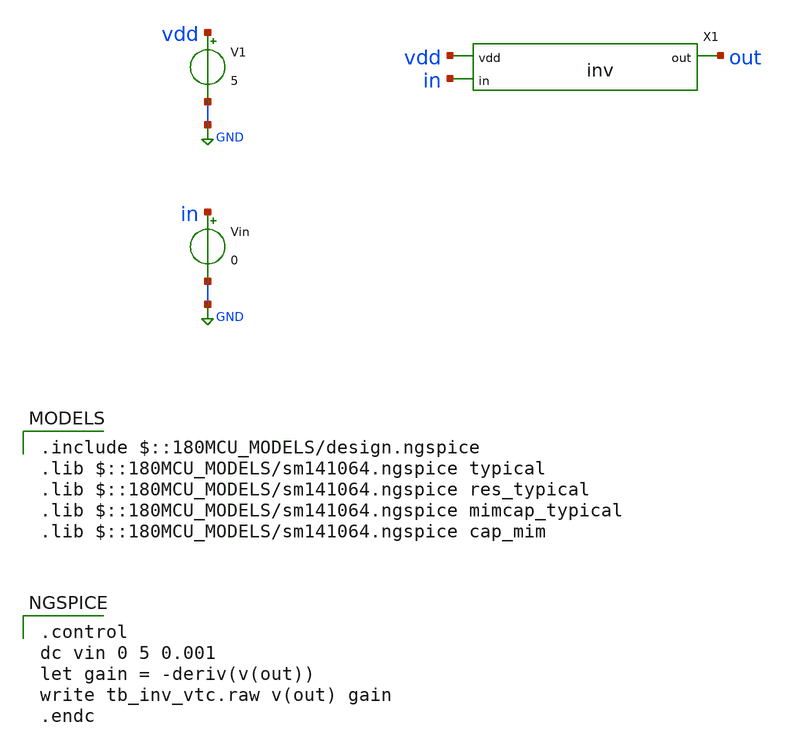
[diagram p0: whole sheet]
** sch_path: Schematics #2/sims/tb/tb_inv_vtc.sch
**.subckt tb_inv_vtc
V1 vdd GND 5
Vin in GND 0
X1 out vdd in inv
**** begin user architecture code
 .include $::180MCU_MODELS/design.ngspice
.lib $::180MCU_MODELS/sm141064.ngspice typical
.lib $::180MCU_MODELS/sm141064.ngspice res_typical
.lib $::180MCU_MODELS/sm141064.ngspice mimcap_typical
.lib $::180MCU_MODELS/sm141064.ngspice cap_mim

.control
dc vin 0 5 0.001
let gain = -deriv(v(out))
write tb_inv_vtc.raw v(out) gain
.endc

**** end user architecture code
**.ends

* expanding   symbol:  xschem/inv.sym # of pins=3
** sym_path: schematic pt2/xschem/inv.sym
** sch_path: schematic pt2/xschem/inv.sch
.subckt inv out vdd in
*.opin out
*.ipin vdd
*.ipin in
XM1 out in gnd GND nfet_03v3 L=0.28u W=wn nf=1 ad='int((nf+1)/2) * W/nf * 0.18u' as='int((nf+2)/2) * W/nf * 0.18u'
+ pd='2*int((nf+1)/2) * (W/nf + 0.18u)' ps='2*int((nf+2)/2) * (W/nf + 0.18u)' nrd='0.18u / W' nrs='0.18u / W'
+ sa=0 sb=0 sd=0 m=1 par=1
XM2 out in vdd VDD pfet_03v3 L=0.28u W=wp nf=1 ad='int((nf+1)/2) * W/nf * 0.18u' as='int((nf+2)/2) * W/nf * 0.18u'
+ pd='2*int((nf+1)/2) * (W/nf + 0.18u)' ps='2*int((nf+2)/2) * (W/nf + 0.18u)' nrd='0.18u / W' nrs='0.18u / W'
+ sa=0 sb=0 sd=0 m=1 par=1
.ends

.GLOBAL GND
.end
